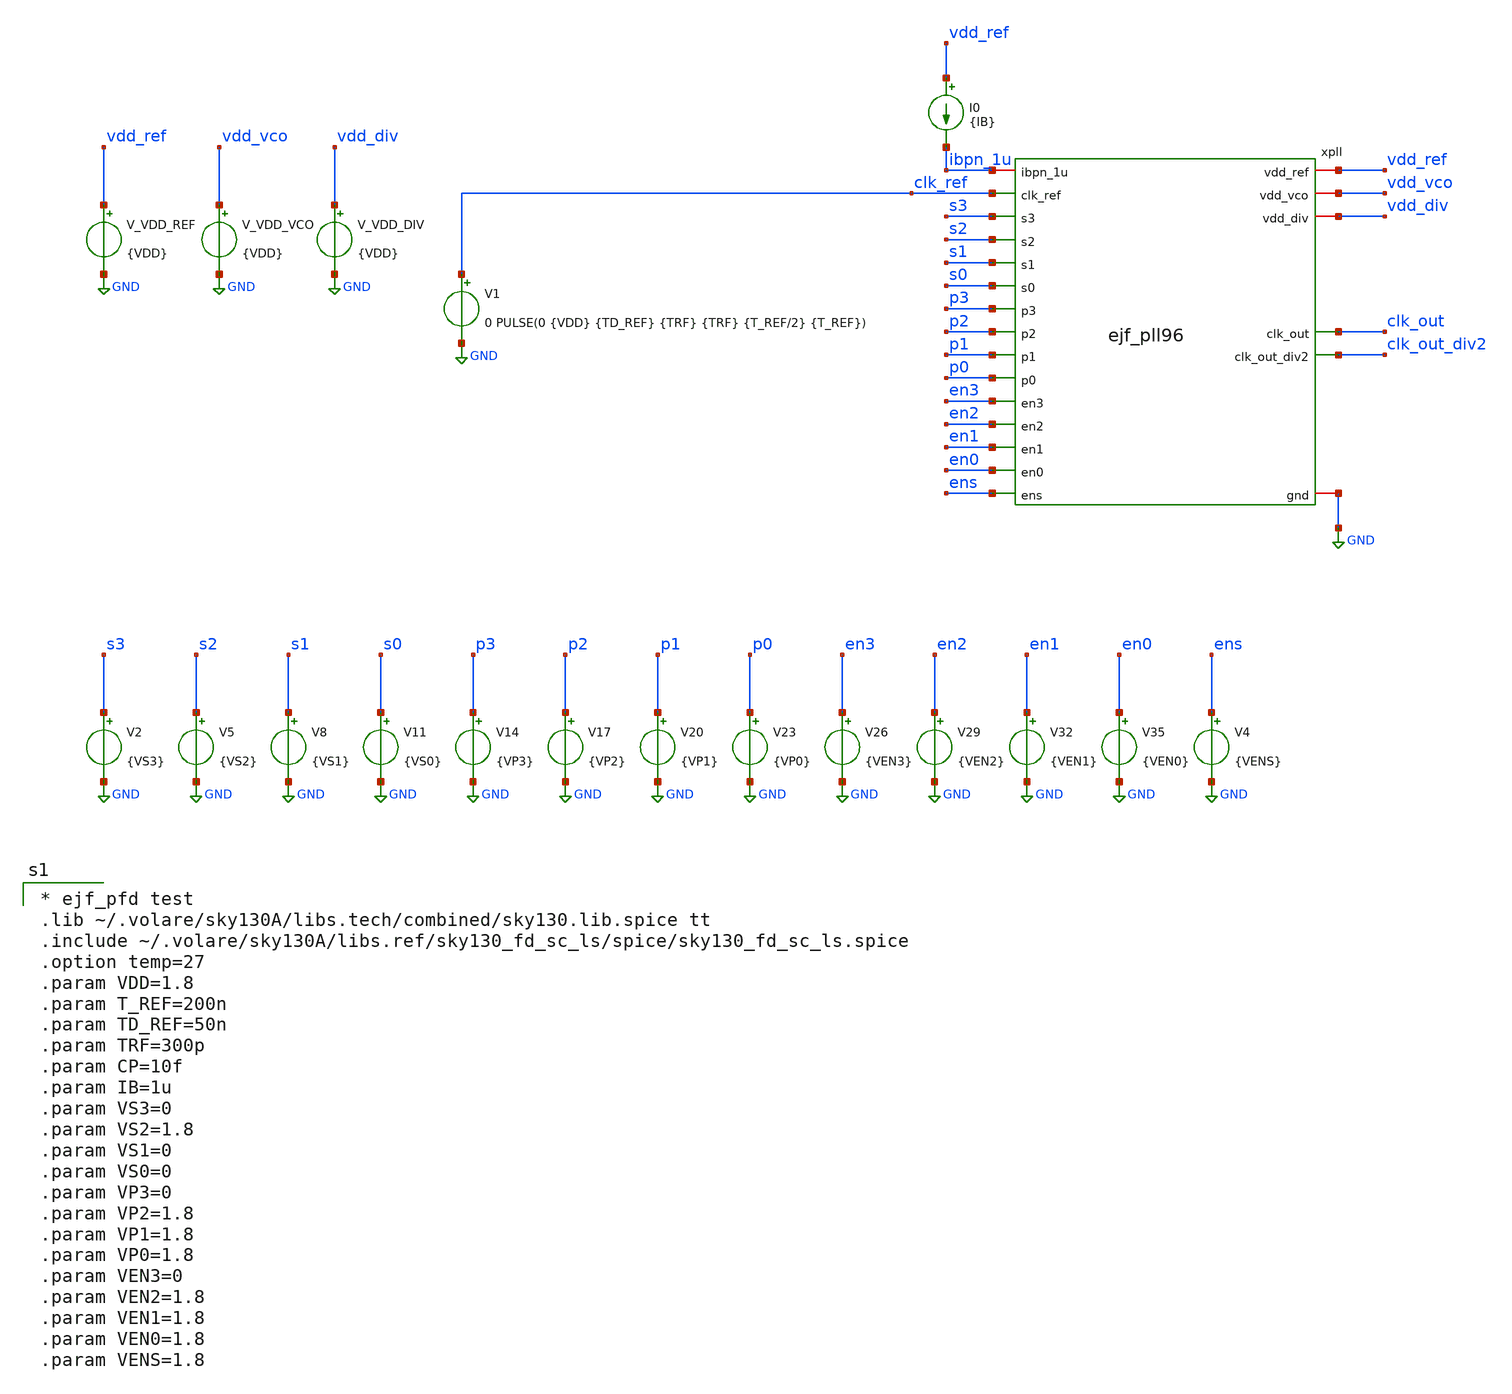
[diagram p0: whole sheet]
** sch_path: xschem/tb_ejf_pll96_top.sch
* xschem/ejf_pll96_diff_buf.sym:
* Copyright (c) 2025 Eric Fogleman
**.subckt tb_ejf_pll96_top
V_VDD_REF vdd_ref GND {VDD}
.save i(v_vdd_ref)
V1 clk_ref GND 0 PULSE(0 {VDD} {TD_REF} {TRF} {TRF} {T_REF/2} {T_REF})
I0 vdd_ref ibpn_1u {IB}
xpll vdd_vco vdd_div vdd_ref clk_ref s3 s2 s1 s0 p3 p2 clk_out p1 p0 en3 en2 en1 en0 ens GND ibpn_1u
+ clk_out_div2 ejf_pll96
V_VDD_VCO vdd_vco GND {VDD}
.save i(v_vdd_vco)
V_VDD_DIV vdd_div GND {VDD}
.save i(v_vdd_div)
V2 s3 GND {VS3}
V5 s2 GND {VS2}
V8 s1 GND {VS1}
V11 s0 GND {VS0}
V14 p3 GND {VP3}
V17 p2 GND {VP2}
V20 p1 GND {VP1}
V23 p0 GND {VP0}
V26 en3 GND {VEN3}
V29 en2 GND {VEN2}
V32 en1 GND {VEN1}
V35 en0 GND {VEN0}
V4 ens GND {VENS}
**** begin user architecture code

* ejf_pfd test
.lib ~/.volare/sky130A/libs.tech/combined/sky130.lib.spice tt
.include ~/.volare/sky130A/libs.ref/sky130_fd_sc_ls/spice/sky130_fd_sc_ls.spice
.option temp=27
.param VDD=1.8
.param T_REF=200n
.param TD_REF=50n
.param TRF=300p
.param CP=10f
.param IB=1u
.param VS3=0
.param VS2=1.8
.param VS1=0
.param VS0=0
.param VP3=0
.param VP2=1.8
.param VP1=1.8
.param VP0=1.8
.param VEN3=0
.param VEN2=1.8
.param VEN1=1.8
.param VEN0=1.8
.param VENS=1.8



* Run transient
* default reltol=1e-3 vntol=1e-6 abstol=1e-12
.options  reltol=1e-4 vntol=1e-7 abstol=1e-13
.options klu
.control
   save i(v_vdd_ref) i(v_vdd_vco) i(v_vdd_div)
   save clk_ref clk_out clk_out_div2
   save xpll.qref xpll.qref_b xpll.qclk xpll.qclk_b xpll.vc xpll.vco_outp xpll.vco_outn
   save xpll.xvco.vhi xpll.xvco.x0p xpll.xvco.x0n xpll.xvco.x1p xpll.xvco.x1n xpll.xvco.x2p
+ xpll.xvco.x2n xpll.xvco.x3p xpll.xvco.x3n xpll.clk_divf
   save xpll.xchp.cp_replica xpll.xchp.mp1g xpll.xchp.mp1cg xpll.xchp.mn1g ibpn_1u xpll.xchp.ng
+ xpll.xchp.mp3d
   save xpll.xlpf.mpc2g
   tran 1n 30u
   write tb_ejf_pll96_top.raw
   meas tran idd_ref avg i(v_vdd_ref) from=18u to=20u
   meas tran idd_vco avg i(v_vdd_vco) from=18u to=20u
   meas tran idd_div avg i(v_vdd_div) from=18u to=20u
   plot xpll.vc
.endc
.end

**** end user architecture code
**.ends

* expanding   symbol:  ejf_pll96.sym # of pins=21
** sym_path: xschem/ejf_pll96.sym
** sch_path: xschem/ejf_pll96.sch
.subckt ejf_pll96 vdd_vco vdd_div vdd_ref clk_ref s3 s2 s1 s0 p3 p2 clk_out p1 p0 en3 en2 en1 en0
+ ens gnd ibpn_1u clk_out_div2
*.iopin vdd_ref
*.iopin vdd_vco
*.iopin vdd_div
*.iopin gnd
*.iopin ibpn_1u
*.ipin clk_ref
*.ipin s3
*.ipin s2
*.ipin s1
*.ipin s0
*.ipin p3
*.ipin p2
*.ipin p1
*.ipin p0
*.ipin en3
*.ipin en2
*.ipin en1
*.ipin en0
*.ipin ens
*.opin clk_out
*.opin clk_out_div2
xlpf vdd_vco vc ejf_pll96_lpf
xdiv p3 vco_outp p2 p1 clk_divf p0 en3 en2 en1 s3 s2 s1 s0 vdd_div gnd en0 ens ejf_pll96_div_mm
xpfd qref clk_ref qclk clk_divf vdd_ref gnd qref_b qclk_b ejf_pll96_pfd
xchp vdd_ref qclk_b qclk vc ibpn_1u qref_b qref gnd ejf_pll96_chp
xvco vdd_vco vc vdd_div vco_outp vco_outn gnd ejf_pll96_vco
x1 vco_outp clk_out clk_out_div2 vdd_div gnd ejf_pll96_outbuf
.ends


* expanding   symbol:  ejf_pll96_lpf.sym # of pins=2
** sym_path: xschem/ejf_pll96_lpf.sym
** sch_path: xschem/ejf_pll96_lpf.sch
.subckt ejf_pll96_lpf vdd vc
*.iopin vc
*.iopin vdd
XR1 net1 net2 vdd sky130_fd_pr__res_high_po_0p69 L=14 mult=1 m=1
XR2 net2 net3 vdd sky130_fd_pr__res_high_po_0p69 L=14 mult=1 m=1
XR3 net3 net4 vdd sky130_fd_pr__res_high_po_0p69 L=14 mult=1 m=1
XR4 net4 net5 vdd sky130_fd_pr__res_high_po_0p69 L=14 mult=1 m=1
XR5 net5 mpc2g vdd sky130_fd_pr__res_high_po_0p69 L=14 mult=1 m=1
XR6 vc net6 vdd sky130_fd_pr__res_high_po_0p69 L=14 mult=1 m=1
XR7 net6 net7 vdd sky130_fd_pr__res_high_po_0p69 L=14 mult=1 m=1
XR8 net7 net8 vdd sky130_fd_pr__res_high_po_0p69 L=14 mult=1 m=1
XR9 net8 net9 vdd sky130_fd_pr__res_high_po_0p69 L=14 mult=1 m=1
XR10 net9 net1 vdd sky130_fd_pr__res_high_po_0p69 L=14 mult=1 m=1
XMPC2 vdd mpc2g vdd vdd sky130_fd_pr__pfet_01v8_lvt L=4 W=4 nf=1 ad='int((nf+1)/2) * W/nf * 0.29' as='int((nf+2)/2) * W/nf * 0.29'
+ pd='2*int((nf+1)/2) * (W/nf + 0.29)' ps='2*int((nf+2)/2) * (W/nf + 0.29)' nrd='0.29 / W' nrs='0.29 / W'
+ sa=0 sb=0 sd=0 mult=280 m=280
XMPC1 vdd vc vdd vdd sky130_fd_pr__pfet_01v8_lvt L=4 W=4 nf=1 ad='int((nf+1)/2) * W/nf * 0.29' as='int((nf+2)/2) * W/nf * 0.29'
+ pd='2*int((nf+1)/2) * (W/nf + 0.29)' ps='2*int((nf+2)/2) * (W/nf + 0.29)' nrd='0.29 / W' nrs='0.29 / W'
+ sa=0 sb=0 sd=0 mult=28 m=28
.ends


* expanding   symbol:  ejf_pll96_div_mm.sym # of pins=17
** sym_path: xschem/ejf_pll96_div_mm.sym
** sch_path: xschem/ejf_pll96_div_mm.sch
.subckt ejf_pll96_div_mm p3 clk p2 p1 q p0 en3 en2 en1 s3 s2 s1 s0 vdd gnd en0 ens
*.iopin gnd
*.ipin clk
*.opin q
*.iopin vdd
*.ipin p3
*.ipin p2
*.ipin p1
*.ipin p0
*.ipin en3
*.ipin en2
*.ipin en1
*.ipin s0
*.ipin s1
*.ipin s2
*.ipin s3
*.ipin ens
*.ipin en0
xn clk_div23 clk mc vdd gnd vdd ejf_pll96_div23
xp clk_div23 p0 en1 p1 q en2 p2 en3 p3 vdd gnd en0 ejf_pll96_div_p
xs clk_div23 s0 s1 s3 s2 q mc vdd gnd ens ejf_pll96_div_s
.ends


* expanding   symbol:  ejf_pll96_pfd.sym # of pins=8
** sym_path: xschem/ejf_pll96_pfd.sym
** sch_path: xschem/ejf_pll96_pfd.sch
.subckt ejf_pll96_pfd qa a qb b vdd gnd qa_b qb_b
*.iopin vdd
*.iopin gnd
*.ipin a
*.ipin b
*.opin qa
*.opin qb
*.opin qa_b
*.opin qb_b
x3 a_b b_b gnd gnd vdd vdd y_par sky130_fd_sc_ls__nor2_2
x4 net1 gnd gnd vdd vdd rst_b sky130_fd_sc_ls__clkinv_1
x1 a vdd rst_b gnd gnd vdd vdd qa0 sky130_fd_sc_ls__dfrtp_2
x2 b vdd rst_b gnd gnd vdd vdd qb0 sky130_fd_sc_ls__dfrtp_2
x6 vdd qa0 qa_b qa gnd a_b ejf_pll96_diff_buf
x7 vdd qb0 qb_b qb gnd b_b ejf_pll96_diff_buf
x8 b_b a_b gnd gnd vdd vdd y_par sky130_fd_sc_ls__nor2_2
x10 y_par gnd gnd vdd vdd net2 sky130_fd_sc_ls__dlygate4sd3_1
x5 net2 gnd gnd vdd vdd net1 sky130_fd_sc_ls__dlygate4sd3_1
**** begin user architecture code

* Copyright (c) Eric Fogleman 2025
* SPDX-License-Identifier: Apache-2.0

**** end user architecture code
.ends


* expanding   symbol:  ejf_pll96_chp.sym # of pins=8
** sym_path: xschem/ejf_pll96_chp.sym
** sch_path: xschem/ejf_pll96_chp.sch
.subckt ejf_pll96_chp vdd p_b p cp ibpn_1u n_b n gnd
*.iopin vdd
*.iopin gnd
*.iopin ibpn_1u
*.iopin cp
*.ipin p
*.ipin n_b
*.ipin p_b
*.ipin n
XMN3 net1 mn1g gnd gnd sky130_fd_pr__nfet_01v8 L=0.5 W=1 nf=1 ad='int((nf+1)/2) * W/nf * 0.29' as='int((nf+2)/2) * W/nf * 0.29'
+ pd='2*int((nf+1)/2) * (W/nf + 0.29)' ps='2*int((nf+2)/2) * (W/nf + 0.29)' nrd='0.29 / W' nrs='0.29 / W'
+ sa=0 sb=0 sd=0 mult=1 m=1
XMN3C mn1g ibpn_1u net1 gnd sky130_fd_pr__nfet_01v8 L=0.15 W=1 nf=1 ad='int((nf+1)/2) * W/nf * 0.29'
+ as='int((nf+2)/2) * W/nf * 0.29' pd='2*int((nf+1)/2) * (W/nf + 0.29)' ps='2*int((nf+2)/2) * (W/nf + 0.29)'
+ nrd='0.29 / W' nrs='0.29 / W' sa=0 sb=0 sd=0 mult=1 m=1
XMP2 net2 mp1g vdd vdd sky130_fd_pr__pfet_01v8 L=0.5 W=2 nf=1 ad='int((nf+1)/2) * W/nf * 0.29' as='int((nf+2)/2) * W/nf * 0.29'
+ pd='2*int((nf+1)/2) * (W/nf + 0.29)' ps='2*int((nf+2)/2) * (W/nf + 0.29)' nrd='0.29 / W' nrs='0.29 / W'
+ sa=0 sb=0 sd=0 mult=1 m=1
XMN2 net3 mn1g gnd gnd sky130_fd_pr__nfet_01v8 L=0.5 W=1 nf=1 ad='int((nf+1)/2) * W/nf * 0.29' as='int((nf+2)/2) * W/nf * 0.29'
+ pd='2*int((nf+1)/2) * (W/nf + 0.29)' ps='2*int((nf+2)/2) * (W/nf + 0.29)' nrd='0.29 / W' nrs='0.29 / W'
+ sa=0 sb=0 sd=0 mult=1 m=1
XMN2C mp1cg ibpn_1u net3 gnd sky130_fd_pr__nfet_01v8 L=0.15 W=1 nf=1 ad='int((nf+1)/2) * W/nf * 0.29'
+ as='int((nf+2)/2) * W/nf * 0.29' pd='2*int((nf+1)/2) * (W/nf + 0.29)' ps='2*int((nf+2)/2) * (W/nf + 0.29)'
+ nrd='0.29 / W' nrs='0.29 / W' sa=0 sb=0 sd=0 mult=1 m=1
XMP1 mp1d mp1g vdd vdd sky130_fd_pr__pfet_01v8 L=0.5 W=2 nf=1 ad='int((nf+1)/2) * W/nf * 0.29' as='int((nf+2)/2) * W/nf * 0.29'
+ pd='2*int((nf+1)/2) * (W/nf + 0.29)' ps='2*int((nf+2)/2) * (W/nf + 0.29)' nrd='0.29 / W' nrs='0.29 / W'
+ sa=0 sb=0 sd=0 mult=5 m=5
XMP2C mp1g mp1cg net2 vdd sky130_fd_pr__pfet_01v8 L=0.15 W=2 nf=1 ad='int((nf+1)/2) * W/nf * 0.29' as='int((nf+2)/2) * W/nf * 0.29'
+ pd='2*int((nf+1)/2) * (W/nf + 0.29)' ps='2*int((nf+2)/2) * (W/nf + 0.29)' nrd='0.29 / W' nrs='0.29 / W'
+ sa=0 sb=0 sd=0 mult=1 m=1
XMP1C mp1cd mp1cg mp1d vdd sky130_fd_pr__pfet_01v8 L=0.15 W=2 nf=1 ad='int((nf+1)/2) * W/nf * 0.29' as='int((nf+2)/2) * W/nf * 0.29'
+ pd='2*int((nf+1)/2) * (W/nf + 0.29)' ps='2*int((nf+2)/2) * (W/nf + 0.29)' nrd='0.29 / W' nrs='0.29 / W'
+ sa=0 sb=0 sd=0 mult=5 m=5
XMN1 mn1d mn1g gnd gnd sky130_fd_pr__nfet_01v8 L=0.5 W=1 nf=1 ad='int((nf+1)/2) * W/nf * 0.29' as='int((nf+2)/2) * W/nf * 0.29'
+ pd='2*int((nf+1)/2) * (W/nf + 0.29)' ps='2*int((nf+2)/2) * (W/nf + 0.29)' nrd='0.29 / W' nrs='0.29 / W'
+ sa=0 sb=0 sd=0 mult=5 m=5
XM1C mn1cd ibpn_1u mn1d gnd sky130_fd_pr__nfet_01v8 L=0.15 W=1 nf=1 ad='int((nf+1)/2) * W/nf * 0.29'
+ as='int((nf+2)/2) * W/nf * 0.29' pd='2*int((nf+1)/2) * (W/nf + 0.29)' ps='2*int((nf+2)/2) * (W/nf + 0.29)'
+ nrd='0.29 / W' nrs='0.29 / W' sa=0 sb=0 sd=0 mult=5 m=5
XR1 mn1g net4 gnd sky130_fd_pr__res_xhigh_po W=0.35 L=10 mult=1 m=1
XR2 net4 ibpn_1u gnd sky130_fd_pr__res_xhigh_po W=0.35 L=10 mult=1 m=1
XR3 mp1cg net5 vdd sky130_fd_pr__res_xhigh_po W=0.35 L=10 mult=1 m=1
XR4 net5 mp1g vdd sky130_fd_pr__res_xhigh_po W=0.35 L=10 mult=1 m=1
XMP11 cp_replica p mp1cd vdd sky130_fd_pr__pfet_01v8 L=0.15 W=1 nf=1 ad='int((nf+1)/2) * W/nf * 0.29'
+ as='int((nf+2)/2) * W/nf * 0.29' pd='2*int((nf+1)/2) * (W/nf + 0.29)' ps='2*int((nf+2)/2) * (W/nf + 0.29)'
+ nrd='0.29 / W' nrs='0.29 / W' sa=0 sb=0 sd=0 mult=1 m=1
XMN11 cp_replica n_b mn1cd gnd sky130_fd_pr__nfet_01v8 L=0.15 W=1 nf=1 ad='int((nf+1)/2) * W/nf * 0.29'
+ as='int((nf+2)/2) * W/nf * 0.29' pd='2*int((nf+1)/2) * (W/nf + 0.29)' ps='2*int((nf+2)/2) * (W/nf + 0.29)'
+ nrd='0.29 / W' nrs='0.29 / W' sa=0 sb=0 sd=0 mult=1 m=1
XMP10 cp p_b mp1cd vdd sky130_fd_pr__pfet_01v8 L=0.15 W=1 nf=1 ad='int((nf+1)/2) * W/nf * 0.29' as='int((nf+2)/2) * W/nf * 0.29'
+ pd='2*int((nf+1)/2) * (W/nf + 0.29)' ps='2*int((nf+2)/2) * (W/nf + 0.29)' nrd='0.29 / W' nrs='0.29 / W'
+ sa=0 sb=0 sd=0 mult=1 m=1
XMN10 cp n mn1cd gnd sky130_fd_pr__nfet_01v8 L=0.15 W=1 nf=1 ad='int((nf+1)/2) * W/nf * 0.29' as='int((nf+2)/2) * W/nf * 0.29'
+ pd='2*int((nf+1)/2) * (W/nf + 0.29)' ps='2*int((nf+2)/2) * (W/nf + 0.29)' nrd='0.29 / W' nrs='0.29 / W'
+ sa=0 sb=0 sd=0 mult=1 m=1
XMN4CAP gnd mn1g gnd gnd sky130_fd_pr__nfet_01v8 L=0.5 W=1 nf=1 ad='int((nf+1)/2) * W/nf * 0.29' as='int((nf+2)/2) * W/nf * 0.29'
+ pd='2*int((nf+1)/2) * (W/nf + 0.29)' ps='2*int((nf+2)/2) * (W/nf + 0.29)' nrd='0.29 / W' nrs='0.29 / W'
+ sa=0 sb=0 sd=0 mult=7 m=7
XMP4CAP vdd mp1g vdd vdd sky130_fd_pr__pfet_01v8 L=0.5 W=2 nf=1 ad='int((nf+1)/2) * W/nf * 0.29' as='int((nf+2)/2) * W/nf * 0.29'
+ pd='2*int((nf+1)/2) * (W/nf + 0.29)' ps='2*int((nf+2)/2) * (W/nf + 0.29)' nrd='0.29 / W' nrs='0.29 / W'
+ sa=0 sb=0 sd=0 mult=6 m=6
XMP5CAP vdd mp1cg vdd vdd sky130_fd_pr__pfet_01v8 L=0.5 W=2 nf=1 ad='int((nf+1)/2) * W/nf * 0.29' as='int((nf+2)/2) * W/nf * 0.29'
+ pd='2*int((nf+1)/2) * (W/nf + 0.29)' ps='2*int((nf+2)/2) * (W/nf + 0.29)' nrd='0.29 / W' nrs='0.29 / W'
+ sa=0 sb=0 sd=0 mult=6 m=6
XMN5CAP gnd ibpn_1u gnd gnd sky130_fd_pr__nfet_01v8 L=0.5 W=1 nf=1 ad='int((nf+1)/2) * W/nf * 0.29' as='int((nf+2)/2) * W/nf * 0.29'
+ pd='2*int((nf+1)/2) * (W/nf + 0.29)' ps='2*int((nf+2)/2) * (W/nf + 0.29)' nrd='0.29 / W' nrs='0.29 / W'
+ sa=0 sb=0 sd=0 mult=7 m=7
XMP3 mp3d mp1g vdd vdd sky130_fd_pr__pfet_01v8 L=0.5 W=2 nf=1 ad='int((nf+1)/2) * W/nf * 0.29' as='int((nf+2)/2) * W/nf * 0.29'
+ pd='2*int((nf+1)/2) * (W/nf + 0.29)' ps='2*int((nf+2)/2) * (W/nf + 0.29)' nrd='0.29 / W' nrs='0.29 / W'
+ sa=0 sb=0 sd=0 mult=2 m=2
XMN6 cp_replica ibpn_1u net6 gnd sky130_fd_pr__nfet_01v8 L=0.15 W=1 nf=1 ad='int((nf+1)/2) * W/nf * 0.29'
+ as='int((nf+2)/2) * W/nf * 0.29' pd='2*int((nf+1)/2) * (W/nf + 0.29)' ps='2*int((nf+2)/2) * (W/nf + 0.29)'
+ nrd='0.29 / W' nrs='0.29 / W' sa=0 sb=0 sd=0 mult=1 m=1
XMN7 ng ibpn_1u net7 gnd sky130_fd_pr__nfet_01v8 L=0.15 W=1 nf=1 ad='int((nf+1)/2) * W/nf * 0.29' as='int((nf+2)/2) * W/nf * 0.29'
+ pd='2*int((nf+1)/2) * (W/nf + 0.29)' ps='2*int((nf+2)/2) * (W/nf + 0.29)' nrd='0.29 / W' nrs='0.29 / W'
+ sa=0 sb=0 sd=0 mult=1 m=1
XM1 cp_replica cp_replica mp3d VDD sky130_fd_pr__pfet_01v8_lvt L=0.35 W=4 nf=2 ad='int((nf+1)/2) * W/nf * 0.29'
+ as='int((nf+2)/2) * W/nf * 0.29' pd='2*int((nf+1)/2) * (W/nf + 0.29)' ps='2*int((nf+2)/2) * (W/nf + 0.29)'
+ nrd='0.29 / W' nrs='0.29 / W' sa=0 sb=0 sd=0 mult=1 m=1
XM2 ng cp mp3d VDD sky130_fd_pr__pfet_01v8_lvt L=0.35 W=4 nf=2 ad='int((nf+1)/2) * W/nf * 0.29' as='int((nf+2)/2) * W/nf * 0.29'
+ pd='2*int((nf+1)/2) * (W/nf + 0.29)' ps='2*int((nf+2)/2) * (W/nf + 0.29)' nrd='0.29 / W' nrs='0.29 / W'
+ sa=0 sb=0 sd=0 mult=1 m=1
XM3 net7 ng gnd GND sky130_fd_pr__nfet_01v8_lvt L=0.35 W=2 nf=2 ad='int((nf+1)/2) * W/nf * 0.29' as='int((nf+2)/2) * W/nf * 0.29'
+ pd='2*int((nf+1)/2) * (W/nf + 0.29)' ps='2*int((nf+2)/2) * (W/nf + 0.29)' nrd='0.29 / W' nrs='0.29 / W'
+ sa=0 sb=0 sd=0 mult=1 m=1
XM4 net6 ng gnd GND sky130_fd_pr__nfet_01v8_lvt L=0.35 W=2 nf=2 ad='int((nf+1)/2) * W/nf * 0.29' as='int((nf+2)/2) * W/nf * 0.29'
+ pd='2*int((nf+1)/2) * (W/nf + 0.29)' ps='2*int((nf+2)/2) * (W/nf + 0.29)' nrd='0.29 / W' nrs='0.29 / W'
+ sa=0 sb=0 sd=0 mult=1 m=1
XMPC1 vdd cp_replica vdd vdd sky130_fd_pr__pfet_01v8_lvt L=4 W=4 nf=1 ad='int((nf+1)/2) * W/nf * 0.29'
+ as='int((nf+2)/2) * W/nf * 0.29' pd='2*int((nf+1)/2) * (W/nf + 0.29)' ps='2*int((nf+2)/2) * (W/nf + 0.29)'
+ nrd='0.29 / W' nrs='0.29 / W' sa=0 sb=0 sd=0 mult=28 m=28
.ends


* expanding   symbol:  ejf_pll96_vco.sym # of pins=6
** sym_path: xschem/ejf_pll96_vco.sym
** sch_path: xschem/ejf_pll96_vco.sch
.subckt ejf_pll96_vco vdd_vco vc vdd outp outn gnd
*.ipin vc
*.iopin vdd_vco
*.opin outp
*.iopin gnd
*.iopin vdd
*.opin outn
x1 vhi x1p x1n x0n x0p gnd ejf_pll96_vco_dlycell
x2 vhi x2n x2p x1p x1n gnd ejf_pll96_vco_dlycell
x0 vhi x0n x0p x3n x3p gnd ejf_pll96_vco_dlycell
x3 vhi x3p x3n x2n x2p gnd ejf_pll96_vco_dlycell
xls vdd x3n outp outn x3p gnd ejf_pll96_vco_ls
V_ISRC net1 vhi 0
XM1 net1 vc net2 vdd_vco sky130_fd_pr__pfet_01v8_lvt L=0.42 W=4.2 nf=1 ad='int((nf+1)/2) * W/nf * 0.29'
+ as='int((nf+2)/2) * W/nf * 0.29' pd='2*int((nf+1)/2) * (W/nf + 0.29)' ps='2*int((nf+2)/2) * (W/nf + 0.29)'
+ nrd='0.29 / W' nrs='0.29 / W' sa=0 sb=0 sd=0 mult=10 m=10
XR1 net2 net3 vdd_vco sky130_fd_pr__res_high_po_1p41 L=3.3 mult=1 m=1
XR2 net3 net4 vdd_vco sky130_fd_pr__res_high_po_1p41 L=3.3 mult=1 m=1
XR3 net4 vdd_vco vdd_vco sky130_fd_pr__res_high_po_1p41 L=3.3 mult=1 m=1
.ends


* expanding   symbol:  ejf_pll96_outbuf.sym # of pins=5
** sym_path: xschem/ejf_pll96_outbuf.sym
** sch_path: xschem/ejf_pll96_outbuf.sch
.subckt ejf_pll96_outbuf in out_vco out_vco_div2 vdd gnd
*.ipin in
*.opin out_vco_div2
*.iopin vdd
*.opin out_vco
*.iopin gnd
x1 in gnd gnd vdd vdd out_vco sky130_fd_sc_ls__clkbuf_2
x2 in net1 gnd gnd vdd vdd out_vco_div2 net1 sky130_fd_sc_ls__dfxbp_2
.ends


* expanding   symbol:  ejf_pll96_div23.sym # of pins=6
** sym_path: xschem/ejf_pll96_div23.sym
** sch_path: xschem/ejf_pll96_div23.sch
.subckt ejf_pll96_div23 q2 clk mc vdd gnd en
*.ipin clk
*.ipin mc
*.opin q2
*.iopin vdd
*.iopin gnd
*.ipin en
x3 q1 mc net1 gnd gnd vdd vdd d2 sky130_fd_sc_ls__o21a_1
x1 clk net1 en gnd gnd vdd vdd q1 sky130_fd_sc_ls__dfstp_2
x2 clk d2 en gnd gnd vdd vdd q2 net1 sky130_fd_sc_ls__dfsbp_2
**** begin user architecture code

* Copyright (c) Eric Fogleman 2025
* SPDX-License-Identifier: Apache-2.0

**** end user architecture code
.ends


* expanding   symbol:  ejf_pll96_div_p.sym # of pins=12
** sym_path: xschem/ejf_pll96_div_p.sym
** sch_path: xschem/ejf_pll96_div_p.sch
.subckt ejf_pll96_div_p clk p0 en1 p1 q en2 p2 en3 p3 vdd gnd en0
*.iopin vdd
*.iopin gnd
*.ipin clk
*.ipin p1
*.ipin p2
*.ipin p3
*.ipin en3
*.ipin en2
*.opin q
*.ipin en1
*.ipin en0
*.ipin p0
x0 q0 clk p0 vdd gnd en0 ejf_pll96_div23
x1 q1 q0 p1 vdd gnd en1 ejf_pll96_div23
x2 q2 q1 p2 vdd gnd en2 ejf_pll96_div23
x3 q3 q2 p3 vdd gnd en3 ejf_pll96_div23
x6 q0 q1 q2 q3 gnd gnd vdd vdd eq0123 sky130_fd_sc_ls__and4_2
x4 clk eq0123 en0 gnd gnd vdd vdd q sky130_fd_sc_ls__dfrtp_2
.ends


* expanding   symbol:  ejf_pll96_div_s.sym # of pins=10
** sym_path: xschem/ejf_pll96_div_s.sym
** sch_path: xschem/ejf_pll96_div_s.sch
.subckt ejf_pll96_div_s clk s0 s1 s3 s2 clr q vdd gnd en
*.ipin s0
*.ipin s1
*.ipin s2
*.ipin s3
*.ipin clk
*.iopin vdd
*.iopin gnd
*.ipin en
*.ipin clr
*.opin q
x1 q0 s0 gnd gnd vdd vdd eq0 sky130_fd_sc_ls__xnor2_1
xdff0 clk q0_b q_b gnd gnd vdd vdd q0 q0_b sky130_fd_sc_ls__dfrbp_1
x5 q1 s1 gnd gnd vdd vdd eq1 sky130_fd_sc_ls__xnor2_1
xdff1 q0_b q1_b q_b gnd gnd vdd vdd q1 q1_b sky130_fd_sc_ls__dfrbp_1
x7 q2 s2 gnd gnd vdd vdd eq2 sky130_fd_sc_ls__xnor2_1
xdff2 q1_b q2_b q_b gnd gnd vdd vdd q2 q2_b sky130_fd_sc_ls__dfrbp_1
x9 q3 s3 gnd gnd vdd vdd eq3 sky130_fd_sc_ls__xnor2_1
xdff3 q2_b q3_b q_b gnd gnd vdd vdd q3 q3_b sky130_fd_sc_ls__dfrbp_1
x8 en gnd gnd vdd vdd en_b sky130_fd_sc_ls__inv_1
x4 q eq0123 en_b gnd gnd vdd vdd q_b sky130_fd_sc_ls__nor3_2
x2 eq3 eq2 eq1 eq0 gnd gnd vdd vdd eq0123 sky130_fd_sc_ls__and4_2
x11 en clr q_b gnd gnd vdd vdd q sky130_fd_sc_ls__a21oi_2
.ends


* expanding   symbol:  ejf_pll96_diff_buf.sym # of pins=6
** sym_path: xschem/ejf_pll96_diff_buf.sym
** sch_path: xschem/ejf_pll96_diff_buf.sch
.subckt ejf_pll96_diff_buf vdd a y_b y gnd a_b
*.iopin vdd
*.iopin gnd
*.ipin a
*.opin y_b
*.opin y
*.opin a_b
XM11 a_b a gnd gnd sky130_fd_pr__nfet_01v8 L=0.15 W=0.84 nf=2 ad='int((nf+1)/2) * W/nf * 0.29' as='int((nf+2)/2) * W/nf * 0.29'
+ pd='2*int((nf+1)/2) * (W/nf + 0.29)' ps='2*int((nf+2)/2) * (W/nf + 0.29)' nrd='0.29 / W' nrs='0.29 / W'
+ sa=0 sb=0 sd=0 mult=1 m=1
XM12 a_b a vdd vdd sky130_fd_pr__pfet_01v8_hvt L=0.15 W=3.36 nf=3 ad='int((nf+1)/2) * W/nf * 0.29' as='int((nf+2)/2) * W/nf * 0.29'
+ pd='2*int((nf+1)/2) * (W/nf + 0.29)' ps='2*int((nf+2)/2) * (W/nf + 0.29)' nrd='0.29 / W' nrs='0.29 / W'
+ sa=0 sb=0 sd=0 mult=1 m=1
XM1 y_b net1 gnd gnd sky130_fd_pr__nfet_01v8 L=0.15 W=0.84 nf=2 ad='int((nf+1)/2) * W/nf * 0.29' as='int((nf+2)/2) * W/nf * 0.29'
+ pd='2*int((nf+1)/2) * (W/nf + 0.29)' ps='2*int((nf+2)/2) * (W/nf + 0.29)' nrd='0.29 / W' nrs='0.29 / W'
+ sa=0 sb=0 sd=0 mult=1 m=1
XM2 y_b net1 vdd vdd sky130_fd_pr__pfet_01v8_hvt L=0.15 W=3.36 nf=3 ad='int((nf+1)/2) * W/nf * 0.29'
+ as='int((nf+2)/2) * W/nf * 0.29' pd='2*int((nf+1)/2) * (W/nf + 0.29)' ps='2*int((nf+2)/2) * (W/nf + 0.29)'
+ nrd='0.29 / W' nrs='0.29 / W' sa=0 sb=0 sd=0 mult=1 m=1
XM3 net1 a_b gnd gnd sky130_fd_pr__nfet_01v8 L=0.15 W=0.84 nf=2 ad='int((nf+1)/2) * W/nf * 0.29' as='int((nf+2)/2) * W/nf * 0.29'
+ pd='2*int((nf+1)/2) * (W/nf + 0.29)' ps='2*int((nf+2)/2) * (W/nf + 0.29)' nrd='0.29 / W' nrs='0.29 / W'
+ sa=0 sb=0 sd=0 mult=1 m=1
XM4 net1 a_b vdd vdd sky130_fd_pr__pfet_01v8_hvt L=0.15 W=3.36 nf=3 ad='int((nf+1)/2) * W/nf * 0.29'
+ as='int((nf+2)/2) * W/nf * 0.29' pd='2*int((nf+1)/2) * (W/nf + 0.29)' ps='2*int((nf+2)/2) * (W/nf + 0.29)'
+ nrd='0.29 / W' nrs='0.29 / W' sa=0 sb=0 sd=0 mult=1 m=1
XM5 y net2 gnd gnd sky130_fd_pr__nfet_01v8 L=0.15 W=0.84 nf=2 ad='int((nf+1)/2) * W/nf * 0.29' as='int((nf+2)/2) * W/nf * 0.29'
+ pd='2*int((nf+1)/2) * (W/nf + 0.29)' ps='2*int((nf+2)/2) * (W/nf + 0.29)' nrd='0.29 / W' nrs='0.29 / W'
+ sa=0 sb=0 sd=0 mult=1 m=1
XM6 y net2 vdd vdd sky130_fd_pr__pfet_01v8_hvt L=0.15 W=3.36 nf=3 ad='int((nf+1)/2) * W/nf * 0.29' as='int((nf+2)/2) * W/nf * 0.29'
+ pd='2*int((nf+1)/2) * (W/nf + 0.29)' ps='2*int((nf+2)/2) * (W/nf + 0.29)' nrd='0.29 / W' nrs='0.29 / W'
+ sa=0 sb=0 sd=0 mult=1 m=1
XM9 net2 gnd a_b VDD sky130_fd_pr__pfet_01v8_hvt L=0.15 W=3.36 nf=3 ad='int((nf+1)/2) * W/nf * 0.29'
+ as='int((nf+2)/2) * W/nf * 0.29' pd='2*int((nf+1)/2) * (W/nf + 0.29)' ps='2*int((nf+2)/2) * (W/nf + 0.29)'
+ nrd='0.29 / W' nrs='0.29 / W' sa=0 sb=0 sd=0 mult=1 m=1
XM10 net2 vdd a_b GND sky130_fd_pr__nfet_01v8 L=0.15 W=0.84 nf=2 ad='int((nf+1)/2) * W/nf * 0.29' as='int((nf+2)/2) * W/nf * 0.29'
+ pd='2*int((nf+1)/2) * (W/nf + 0.29)' ps='2*int((nf+2)/2) * (W/nf + 0.29)' nrd='0.29 / W' nrs='0.29 / W'
+ sa=0 sb=0 sd=0 mult=1 m=1
**** begin user architecture code

* Copyright (c) Eric Fogleman 2025
* SPDX-License-Identifier: Apache-2.0

**** end user architecture code
.ends


* expanding   symbol:  ejf_pll96_vco_dlycell.sym # of pins=6
** sym_path: xschem/ejf_pll96_vco_dlycell.sym
** sch_path: xschem/ejf_pll96_vco_dlycell.sch
.subckt ejf_pll96_vco_dlycell vhi outn outp inp inn gnd
*.ipin inp
*.opin outn
*.ipin inn
*.opin outp
*.iopin vhi
*.iopin gnd
XM11 outp outn gnd gnd sky130_fd_pr__nfet_01v8 L=0.44 W=1.22 nf=1 ad='int((nf+1)/2) * W/nf * 0.29' as='int((nf+2)/2) * W/nf * 0.29'
+ pd='2*int((nf+1)/2) * (W/nf + 0.29)' ps='2*int((nf+2)/2) * (W/nf + 0.29)' nrd='0.29 / W' nrs='0.29 / W'
+ sa=0 sb=0 sd=0 mult=1 m=1
XM13 outn inp gnd gnd sky130_fd_pr__nfet_01v8 L=0.44 W=4.88 nf=4 ad='int((nf+1)/2) * W/nf * 0.29' as='int((nf+2)/2) * W/nf * 0.29'
+ pd='2*int((nf+1)/2) * (W/nf + 0.29)' ps='2*int((nf+2)/2) * (W/nf + 0.29)' nrd='0.29 / W' nrs='0.29 / W'
+ sa=0 sb=0 sd=0 mult=1 m=1
XM14 outn inp vhi vhi sky130_fd_pr__pfet_01v8_hvt L=0.44 W=19.44 nf=6 ad='int((nf+1)/2) * W/nf * 0.29'
+ as='int((nf+2)/2) * W/nf * 0.29' pd='2*int((nf+1)/2) * (W/nf + 0.29)' ps='2*int((nf+2)/2) * (W/nf + 0.29)'
+ nrd='0.29 / W' nrs='0.29 / W' sa=0 sb=0 sd=0 mult=1 m=1
XM27 outn outp gnd gnd sky130_fd_pr__nfet_01v8 L=0.44 W=1.22 nf=1 ad='int((nf+1)/2) * W/nf * 0.29' as='int((nf+2)/2) * W/nf * 0.29'
+ pd='2*int((nf+1)/2) * (W/nf + 0.29)' ps='2*int((nf+2)/2) * (W/nf + 0.29)' nrd='0.29 / W' nrs='0.29 / W'
+ sa=0 sb=0 sd=0 mult=1 m=1
XM31 outp inn gnd gnd sky130_fd_pr__nfet_01v8 L=0.44 W=4.88 nf=4 ad='int((nf+1)/2) * W/nf * 0.29' as='int((nf+2)/2) * W/nf * 0.29'
+ pd='2*int((nf+1)/2) * (W/nf + 0.29)' ps='2*int((nf+2)/2) * (W/nf + 0.29)' nrd='0.29 / W' nrs='0.29 / W'
+ sa=0 sb=0 sd=0 mult=1 m=1
XM30 outp inn vhi vhi sky130_fd_pr__pfet_01v8_hvt L=0.44 W=19.44 nf=6 ad='int((nf+1)/2) * W/nf * 0.29'
+ as='int((nf+2)/2) * W/nf * 0.29' pd='2*int((nf+1)/2) * (W/nf + 0.29)' ps='2*int((nf+2)/2) * (W/nf + 0.29)'
+ nrd='0.29 / W' nrs='0.29 / W' sa=0 sb=0 sd=0 mult=1 m=1
C3 inp gnd {CP} m=1
C4 inn gnd {CP} m=1
**** begin user architecture code

* Copyright (c) Eric Fogleman 2025
* SPDX-License-Identifier: Apache-2.0

**** end user architecture code
.ends


* expanding   symbol:  ejf_pll96_vco_ls.sym # of pins=6
** sym_path: xschem/ejf_pll96_vco_ls.sym
** sch_path: xschem/ejf_pll96_vco_ls.sch
.subckt ejf_pll96_vco_ls vdd inp outp outn inn gnd
*.ipin inp
*.opin outn
*.ipin inn
*.opin outp
*.iopin vdd
*.iopin gnd
XM5 net1 ls_outn vdd vdd sky130_fd_pr__pfet_01v8_hvt L=0.15 W=2 nf=1 ad='int((nf+1)/2) * W/nf * 0.29'
+ as='int((nf+2)/2) * W/nf * 0.29' pd='2*int((nf+1)/2) * (W/nf + 0.29)' ps='2*int((nf+2)/2) * (W/nf + 0.29)'
+ nrd='0.29 / W' nrs='0.29 / W' sa=0 sb=0 sd=0 mult=1 m=1
XM1 ls_outn inp gnd gnd sky130_fd_pr__nfet_01v8 L=0.15 W=2 nf=1 ad='int((nf+1)/2) * W/nf * 0.29' as='int((nf+2)/2) * W/nf * 0.29'
+ pd='2*int((nf+1)/2) * (W/nf + 0.29)' ps='2*int((nf+2)/2) * (W/nf + 0.29)' nrd='0.29 / W' nrs='0.29 / W'
+ sa=0 sb=0 sd=0 mult=1 m=1
XM2 ls_outp inn gnd gnd sky130_fd_pr__nfet_01v8 L=0.15 W=2 nf=1 ad='int((nf+1)/2) * W/nf * 0.29' as='int((nf+2)/2) * W/nf * 0.29'
+ pd='2*int((nf+1)/2) * (W/nf + 0.29)' ps='2*int((nf+2)/2) * (W/nf + 0.29)' nrd='0.29 / W' nrs='0.29 / W'
+ sa=0 sb=0 sd=0 mult=1 m=1
XM3 net2 ls_outp vdd vdd sky130_fd_pr__pfet_01v8_hvt L=0.15 W=2 nf=1 ad='int((nf+1)/2) * W/nf * 0.29'
+ as='int((nf+2)/2) * W/nf * 0.29' pd='2*int((nf+1)/2) * (W/nf + 0.29)' ps='2*int((nf+2)/2) * (W/nf + 0.29)'
+ nrd='0.29 / W' nrs='0.29 / W' sa=0 sb=0 sd=0 mult=1 m=1
XM4 ls_outn inp net2 vdd sky130_fd_pr__pfet_01v8_hvt L=0.15 W=2 nf=1 ad='int((nf+1)/2) * W/nf * 0.29'
+ as='int((nf+2)/2) * W/nf * 0.29' pd='2*int((nf+1)/2) * (W/nf + 0.29)' ps='2*int((nf+2)/2) * (W/nf + 0.29)'
+ nrd='0.29 / W' nrs='0.29 / W' sa=0 sb=0 sd=0 mult=1 m=1
XM6 ls_outp inn net1 vdd sky130_fd_pr__pfet_01v8_hvt L=0.15 W=2 nf=1 ad='int((nf+1)/2) * W/nf * 0.29'
+ as='int((nf+2)/2) * W/nf * 0.29' pd='2*int((nf+1)/2) * (W/nf + 0.29)' ps='2*int((nf+2)/2) * (W/nf + 0.29)'
+ nrd='0.29 / W' nrs='0.29 / W' sa=0 sb=0 sd=0 mult=1 m=1
XM7 outn ls_outp gnd gnd sky130_fd_pr__nfet_01v8 L=0.15 W=2 nf=1 ad='int((nf+1)/2) * W/nf * 0.29' as='int((nf+2)/2) * W/nf * 0.29'
+ pd='2*int((nf+1)/2) * (W/nf + 0.29)' ps='2*int((nf+2)/2) * (W/nf + 0.29)' nrd='0.29 / W' nrs='0.29 / W'
+ sa=0 sb=0 sd=0 mult=1 m=1
XM8 outn ls_outp vdd vdd sky130_fd_pr__pfet_01v8_hvt L=0.15 W=4 nf=1 ad='int((nf+1)/2) * W/nf * 0.29'
+ as='int((nf+2)/2) * W/nf * 0.29' pd='2*int((nf+1)/2) * (W/nf + 0.29)' ps='2*int((nf+2)/2) * (W/nf + 0.29)'
+ nrd='0.29 / W' nrs='0.29 / W' sa=0 sb=0 sd=0 mult=1 m=1
XM9 outp ls_outn gnd gnd sky130_fd_pr__nfet_01v8 L=0.15 W=2 nf=1 ad='int((nf+1)/2) * W/nf * 0.29' as='int((nf+2)/2) * W/nf * 0.29'
+ pd='2*int((nf+1)/2) * (W/nf + 0.29)' ps='2*int((nf+2)/2) * (W/nf + 0.29)' nrd='0.29 / W' nrs='0.29 / W'
+ sa=0 sb=0 sd=0 mult=1 m=1
XM10 outp ls_outn vdd vdd sky130_fd_pr__pfet_01v8_hvt L=0.15 W=4 nf=1 ad='int((nf+1)/2) * W/nf * 0.29'
+ as='int((nf+2)/2) * W/nf * 0.29' pd='2*int((nf+1)/2) * (W/nf + 0.29)' ps='2*int((nf+2)/2) * (W/nf + 0.29)'
+ nrd='0.29 / W' nrs='0.29 / W' sa=0 sb=0 sd=0 mult=1 m=1
**** begin user architecture code

* Copyright (c) Eric Fogleman 2025
* SPDX-License-Identifier: Apache-2.0

**** end user architecture code
.ends

.GLOBAL GND
.end
